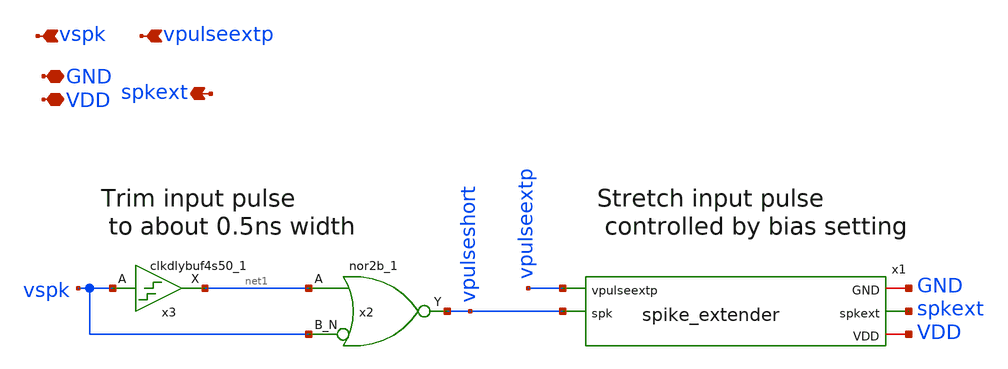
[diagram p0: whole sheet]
** sch_path: design/xschem/spike_extender_with_trimming.sch
**.subckt spike_extender_with_trimming GND VDD vspk spkext vpulseextp
*.iopin GND
*.iopin VDD
*.ipin vspk
*.opin spkext
*.ipin vpulseextp
x1 vpulseextp vpulseshort GND spkext VDD spike_extender
x3 vspk GND GND VDD VDD net1 sky130_fd_sc_hd__clkdlybuf4s50_1
x2 net1 vspk GND GND VDD VDD vpulseshort sky130_fd_sc_hd__nor2b_1
**.ends

* expanding   symbol:  spike_extender.sym # of pins=5
** sym_path: design/xschem/spike_extender.sym
** sch_path: design/xschem/spike_extender.sch
.subckt spike_extender vpulseextp spk GND spkext VDD
*.iopin GND
*.iopin VDD
*.ipin spk
*.opin spkext
*.ipin vpulseextp
XM1 net1 spk GND GND sky130_fd_pr__nfet_01v8 L=0.15 W=0.65 nf=1 ad='int((nf+1)/2) * W/nf * 0.29' as='int((nf+2)/2) * W/nf * 0.29'
+ pd='2*int((nf+1)/2) * (W/nf + 0.29)' ps='2*int((nf+2)/2) * (W/nf + 0.29)' nrd='0.29 / W' nrs='0.29 / W'
+ sa=0 sb=0 sd=0 mult=1 m=1
XM6 net1 vpulseextp VDD VDD sky130_fd_pr__pfet_01v8 L=2 W=1 nf=1 ad='int((nf+1)/2) * W/nf * 0.29' as='int((nf+2)/2) * W/nf * 0.29'
+ pd='2*int((nf+1)/2) * (W/nf + 0.29)' ps='2*int((nf+2)/2) * (W/nf + 0.29)' nrd='0.29 / W' nrs='0.29 / W'
+ sa=0 sb=0 sd=0 mult=1 m=1
XM5 net3 net2 GND GND sky130_fd_pr__nfet_01v8 L=0.15 W=0.65 nf=1 ad='int((nf+1)/2) * W/nf * 0.29' as='int((nf+2)/2) * W/nf * 0.29'
+ pd='2*int((nf+1)/2) * (W/nf + 0.29)' ps='2*int((nf+2)/2) * (W/nf + 0.29)' nrd='0.29 / W' nrs='0.29 / W'
+ sa=0 sb=0 sd=0 mult=1 m=1
XM8 spkext net3 GND GND sky130_fd_pr__nfet_01v8 L=0.15 W=0.65 nf=1 ad='int((nf+1)/2) * W/nf * 0.29' as='int((nf+2)/2) * W/nf * 0.29'
+ pd='2*int((nf+1)/2) * (W/nf + 0.29)' ps='2*int((nf+2)/2) * (W/nf + 0.29)' nrd='0.29 / W' nrs='0.29 / W'
+ sa=0 sb=0 sd=0 mult=1 m=1
XM4 net3 net2 VDD VDD sky130_fd_pr__pfet_01v8 L=0.15 W=1.0 nf=1 ad='int((nf+1)/2) * W/nf * 0.29' as='int((nf+2)/2) * W/nf * 0.29'
+ pd='2*int((nf+1)/2) * (W/nf + 0.29)' ps='2*int((nf+2)/2) * (W/nf + 0.29)' nrd='0.29 / W' nrs='0.29 / W'
+ sa=0 sb=0 sd=0 mult=1 m=1
XM7 spkext net3 VDD VDD sky130_fd_pr__pfet_01v8 L=0.15 W=1.0 nf=1 ad='int((nf+1)/2) * W/nf * 0.29' as='int((nf+2)/2) * W/nf * 0.29'
+ pd='2*int((nf+1)/2) * (W/nf + 0.29)' ps='2*int((nf+2)/2) * (W/nf + 0.29)' nrd='0.29 / W' nrs='0.29 / W'
+ sa=0 sb=0 sd=0 mult=1 m=1
XM2 net2 net1 GND GND sky130_fd_pr__nfet_01v8 L=0.15 W=0.65 nf=1 ad='int((nf+1)/2) * W/nf * 0.29' as='int((nf+2)/2) * W/nf * 0.29'
+ pd='2*int((nf+1)/2) * (W/nf + 0.29)' ps='2*int((nf+2)/2) * (W/nf + 0.29)' nrd='0.29 / W' nrs='0.29 / W'
+ sa=0 sb=0 sd=0 mult=1 m=1
XM3 net2 net1 VDD VDD sky130_fd_pr__pfet_01v8 L=0.15 W=1.0 nf=1 ad='int((nf+1)/2) * W/nf * 0.29' as='int((nf+2)/2) * W/nf * 0.29'
+ pd='2*int((nf+1)/2) * (W/nf + 0.29)' ps='2*int((nf+2)/2) * (W/nf + 0.29)' nrd='0.29 / W' nrs='0.29 / W'
+ sa=0 sb=0 sd=0 mult=1 m=1
XM9 GND net1 GND GND sky130_fd_pr__nfet_01v8 L=1 W=0.65 nf=1 ad='int((nf+1)/2) * W/nf * 0.29' as='int((nf+2)/2) * W/nf * 0.29'
+ pd='2*int((nf+1)/2) * (W/nf + 0.29)' ps='2*int((nf+2)/2) * (W/nf + 0.29)' nrd='0.29 / W' nrs='0.29 / W'
+ sa=0 sb=0 sd=0 mult=1 m=1
.ends

.end
